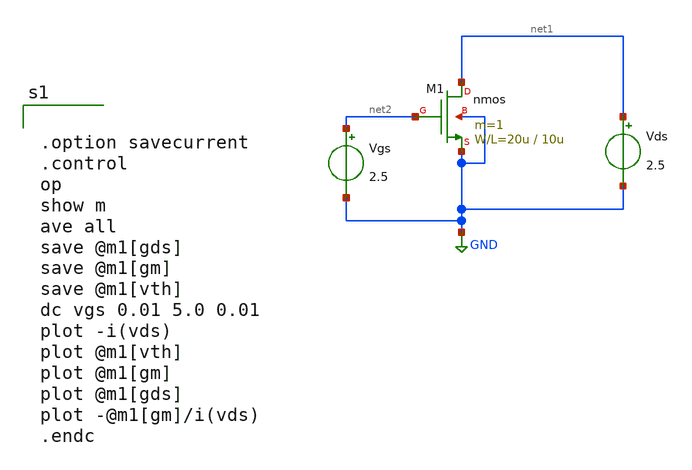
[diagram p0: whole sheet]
** sch_path: member_project/GroupWork/Team_masahiro/nfet_id-vgs_2l.sch
**.subckt nfet_id-vgs_2l
M1 net1 net2 GND GND nmos L=10u W=20u m=1
Vgs net2 GND 2.5
Vds net1 GND 2.5
**** begin user architecture code
 .include $::LIB/mos.lib
.include $::LIB/passive.lib
.include $::LIB/diode.lib


.option savecurrent
.control
op
show m
ave all
save @m1[gds]
save @m1[gm]
save @m1[vth]
dc vgs 0.01 5.0 0.01
plot -i(vds)
plot @m1[vth]
plot @m1[gm]
plot @m1[gds]
plot -@m1[gm]/i(vds)
.endc


**** end user architecture code
**.ends
.GLOBAL GND
.end
